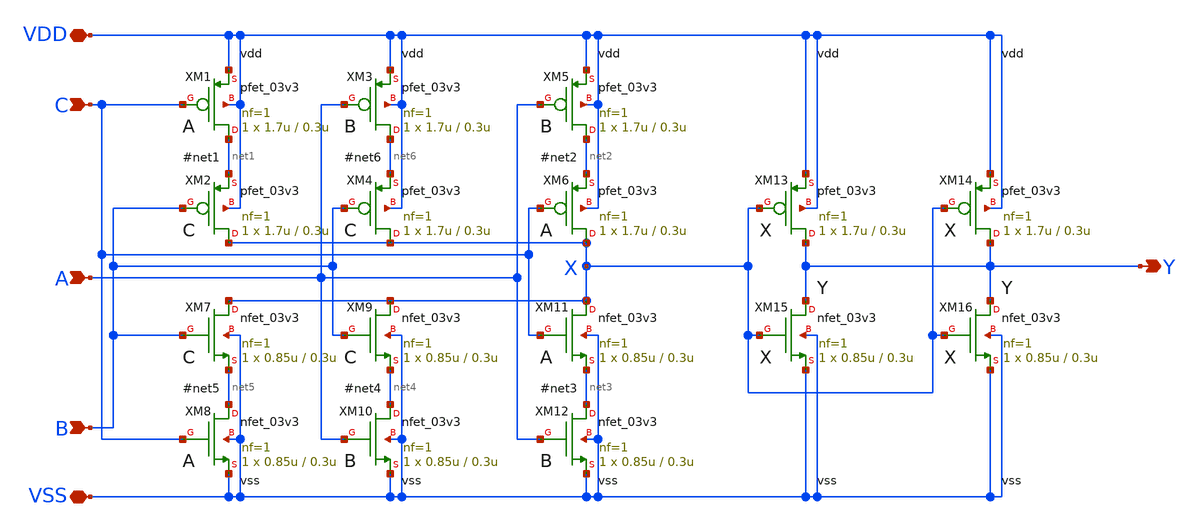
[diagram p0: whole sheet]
** sch_path: lvs/gf180mcu_osu_sc_gp9t3v3__maj3.sch
**.subckt gf180mcu_osu_sc_gp9t3v3__maj3 VDD VSS A B C Y
*.iopin VDD
*.iopin VSS
*.ipin A
*.ipin B
*.ipin C
*.opin Y
XM1 net1 C VDD VDD pfet_03v3 L=0.3u W=1.7u nf=1 ad='int((nf+1)/2) * W/nf * 0.18u' as='int((nf+2)/2) * W/nf * 0.18u'
+ pd='2*int((nf+1)/2) * (W/nf + 0.18u)' ps='2*int((nf+2)/2) * (W/nf + 0.18u)' nrd='0.18u / W' nrs='0.18u / W'
+ sa=0 sb=0 sd=0 m=1
XM2 X B net1 VDD pfet_03v3 L=0.3u W=1.7u nf=1 ad='int((nf+1)/2) * W/nf * 0.18u' as='int((nf+2)/2) * W/nf * 0.18u'
+ pd='2*int((nf+1)/2) * (W/nf + 0.18u)' ps='2*int((nf+2)/2) * (W/nf + 0.18u)' nrd='0.18u / W' nrs='0.18u / W'
+ sa=0 sb=0 sd=0 m=1
XM3 net6 A VDD VDD pfet_03v3 L=0.3u W=1.7u nf=1 ad='int((nf+1)/2) * W/nf * 0.18u' as='int((nf+2)/2) * W/nf * 0.18u'
+ pd='2*int((nf+1)/2) * (W/nf + 0.18u)' ps='2*int((nf+2)/2) * (W/nf + 0.18u)' nrd='0.18u / W' nrs='0.18u / W'
+ sa=0 sb=0 sd=0 m=1
XM5 net2 A VDD VDD pfet_03v3 L=0.3u W=1.7u nf=1 ad='int((nf+1)/2) * W/nf * 0.18u' as='int((nf+2)/2) * W/nf * 0.18u'
+ pd='2*int((nf+1)/2) * (W/nf + 0.18u)' ps='2*int((nf+2)/2) * (W/nf + 0.18u)' nrd='0.18u / W' nrs='0.18u / W'
+ sa=0 sb=0 sd=0 m=1
XM6 X C net2 VDD pfet_03v3 L=0.3u W=1.7u nf=1 ad='int((nf+1)/2) * W/nf * 0.18u' as='int((nf+2)/2) * W/nf * 0.18u'
+ pd='2*int((nf+1)/2) * (W/nf + 0.18u)' ps='2*int((nf+2)/2) * (W/nf + 0.18u)' nrd='0.18u / W' nrs='0.18u / W'
+ sa=0 sb=0 sd=0 m=1
XM4 X B net6 VDD pfet_03v3 L=0.3u W=1.7u nf=1 ad='int((nf+1)/2) * W/nf * 0.18u' as='int((nf+2)/2) * W/nf * 0.18u'
+ pd='2*int((nf+1)/2) * (W/nf + 0.18u)' ps='2*int((nf+2)/2) * (W/nf + 0.18u)' nrd='0.18u / W' nrs='0.18u / W'
+ sa=0 sb=0 sd=0 m=1
XM7 X B net5 VSS nfet_03v3 L=0.3u W=0.85u nf=1 ad='int((nf+1)/2) * W/nf * 0.18u' as='int((nf+2)/2) * W/nf * 0.18u'
+ pd='2*int((nf+1)/2) * (W/nf + 0.18u)' ps='2*int((nf+2)/2) * (W/nf + 0.18u)' nrd='0.18u / W' nrs='0.18u / W'
+ sa=0 sb=0 sd=0 m=1
XM8 net5 C VSS VSS nfet_03v3 L=0.3u W=0.85u nf=1 ad='int((nf+1)/2) * W/nf * 0.18u' as='int((nf+2)/2) * W/nf * 0.18u'
+ pd='2*int((nf+1)/2) * (W/nf + 0.18u)' ps='2*int((nf+2)/2) * (W/nf + 0.18u)' nrd='0.18u / W' nrs='0.18u / W'
+ sa=0 sb=0 sd=0 m=1
XM9 X B net4 VSS nfet_03v3 L=0.3u W=0.85u nf=1 ad='int((nf+1)/2) * W/nf * 0.18u' as='int((nf+2)/2) * W/nf * 0.18u'
+ pd='2*int((nf+1)/2) * (W/nf + 0.18u)' ps='2*int((nf+2)/2) * (W/nf + 0.18u)' nrd='0.18u / W' nrs='0.18u / W'
+ sa=0 sb=0 sd=0 m=1
XM10 net4 A VSS VSS nfet_03v3 L=0.3u W=0.85u nf=1 ad='int((nf+1)/2) * W/nf * 0.18u' as='int((nf+2)/2) * W/nf * 0.18u'
+ pd='2*int((nf+1)/2) * (W/nf + 0.18u)' ps='2*int((nf+2)/2) * (W/nf + 0.18u)' nrd='0.18u / W' nrs='0.18u / W'
+ sa=0 sb=0 sd=0 m=1
XM11 X C net3 VSS nfet_03v3 L=0.3u W=0.85u nf=1 ad='int((nf+1)/2) * W/nf * 0.18u' as='int((nf+2)/2) * W/nf * 0.18u'
+ pd='2*int((nf+1)/2) * (W/nf + 0.18u)' ps='2*int((nf+2)/2) * (W/nf + 0.18u)' nrd='0.18u / W' nrs='0.18u / W'
+ sa=0 sb=0 sd=0 m=1
XM12 net3 A VSS VSS nfet_03v3 L=0.3u W=0.85u nf=1 ad='int((nf+1)/2) * W/nf * 0.18u' as='int((nf+2)/2) * W/nf * 0.18u'
+ pd='2*int((nf+1)/2) * (W/nf + 0.18u)' ps='2*int((nf+2)/2) * (W/nf + 0.18u)' nrd='0.18u / W' nrs='0.18u / W'
+ sa=0 sb=0 sd=0 m=1
XM13 Y X VDD VDD pfet_03v3 L=0.3u W=1.7u nf=1 ad='int((nf+1)/2) * W/nf * 0.18u' as='int((nf+2)/2) * W/nf * 0.18u'
+ pd='2*int((nf+1)/2) * (W/nf + 0.18u)' ps='2*int((nf+2)/2) * (W/nf + 0.18u)' nrd='0.18u / W' nrs='0.18u / W'
+ sa=0 sb=0 sd=0 m=1
XM14 Y X VDD VDD pfet_03v3 L=0.3u W=1.7u nf=1 ad='int((nf+1)/2) * W/nf * 0.18u' as='int((nf+2)/2) * W/nf * 0.18u'
+ pd='2*int((nf+1)/2) * (W/nf + 0.18u)' ps='2*int((nf+2)/2) * (W/nf + 0.18u)' nrd='0.18u / W' nrs='0.18u / W'
+ sa=0 sb=0 sd=0 m=1
XM15 Y X VSS VSS nfet_03v3 L=0.3u W=0.85u nf=1 ad='int((nf+1)/2) * W/nf * 0.18u' as='int((nf+2)/2) * W/nf * 0.18u'
+ pd='2*int((nf+1)/2) * (W/nf + 0.18u)' ps='2*int((nf+2)/2) * (W/nf + 0.18u)' nrd='0.18u / W' nrs='0.18u / W'
+ sa=0 sb=0 sd=0 m=1
XM16 Y X VSS VSS nfet_03v3 L=0.3u W=0.85u nf=1 ad='int((nf+1)/2) * W/nf * 0.18u' as='int((nf+2)/2) * W/nf * 0.18u'
+ pd='2*int((nf+1)/2) * (W/nf + 0.18u)' ps='2*int((nf+2)/2) * (W/nf + 0.18u)' nrd='0.18u / W' nrs='0.18u / W'
+ sa=0 sb=0 sd=0 m=1
**.ends
.end
